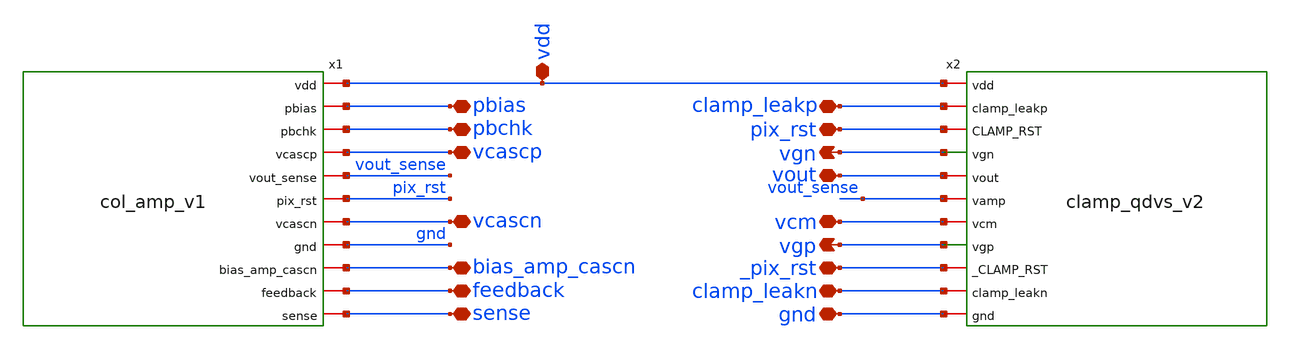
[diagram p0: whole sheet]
** sch_path: analog/xschem/col_amp_n_clamp_v1/analog_column_layout_schem.sch
**.subckt analog_column_layout_schem clamp_leakn gnd vdd vgn clamp_leakp vgp vcm vout pix_rst
*+ _pix_rst sense pbchk vcascp pbias feedback vcascn bias_amp_cascn
*.iopin clamp_leakn
*.iopin gnd
*.iopin vdd
*.opin vgn
*.iopin clamp_leakp
*.opin vgp
*.iopin vcm
*.iopin vout
*.iopin pix_rst
*.iopin _pix_rst
*.iopin sense
*.iopin pbchk
*.iopin vcascp
*.iopin pbias
*.iopin feedback
*.iopin vcascn
*.iopin bias_amp_cascn
x1 vdd pbias pbchk vcascp vout_sense pix_rst vcascn gnd bias_amp_cascn feedback sense col_amp_v1
x2 vdd clamp_leakp pix_rst vgn vout vout_sense vcm vgp _pix_rst clamp_leakn gnd clamp_qdvs_v2
**.ends

* expanding   symbol:
*+  /home/user/projects/nic2025_v2/nic2025_openDVS/analog/xschem/col_amp_n_clamp_v1/col_amp_v1.sym # of pins=11
** sym_path: analog/xschem/col_amp_n_clamp_v1/col_amp_v1.sym
** sch_path: analog/xschem/col_amp_n_clamp_v1/col_amp_v1.sch
.subckt col_amp_v1 vdd pbias pbchk vcascp vout_sense pix_rst vcascn gnd bias_amp_cascn feedback
+ sense
*.iopin vdd
*.iopin gnd
*.iopin sense
*.iopin vout_sense
*.iopin feedback
*.iopin pbchk
*.iopin pix_rst
*.iopin vcascn
*.iopin vcascp
*.iopin pbias
*.iopin bias_amp_cascn
XMpb pbchk pbias vdd vdd sky130_fd_pr__pfet_01v8 L=1 W=1.25 nf=1 ad='int((1 + 1)/2) * 1.25 / 1 * 0.29'
+ as='int((1 + 2)/2) * 1.25 / 1 * 0.29' pd='2*int((1 + 1)/2) * (1.25 / 1 + 0.29)' ps='2*int((1 + 2)/2) * (1.25 / 1 + 0.29)'
+ nrd='0.29 / 1.25 ' nrs='0.29 / 1.25 ' sa=0 sb=0 sd=0 mult=1 m=1
XMnc vout_sense amp_p_vg sense gnd sky130_fd_pr__nfet_01v8 L=1 W=0.75 nf=1 ad='int((1 + 1)/2) * 0.75 / 1 * 0.29'
+ as='int((1 + 2)/2) * 0.75 / 1 * 0.29' pd='2*int((1 + 1)/2) * (0.75 / 1 + 0.29)' ps='2*int((1 + 2)/2) * (0.75 / 1 + 0.29)'
+ nrd='0.29 / 0.75 ' nrs='0.29 / 0.75 ' sa=0 sb=0 sd=0 mult=1 m=1
XMfb vout_sense pix_rst feedback gnd sky130_fd_pr__nfet_01v8 L=0.5 W=0.5 nf=1 ad='int((1 + 1)/2) * 0.5 / 1 * 0.29'
+ as='int((1 + 2)/2) * 0.5 / 1 * 0.29' pd='2*int((1 + 1)/2) * (0.5 / 1 + 0.29)' ps='2*int((1 + 2)/2) * (0.5 / 1 + 0.29)'
+ nrd='0.29 / 0.5 ' nrs='0.29 / 0.5 ' sa=0 sb=0 sd=0 mult=1 m=1
XMpc vout_sense vcascp pbchk vdd sky130_fd_pr__pfet_01v8 L=1 W=1.25 nf=1 ad='int((1 + 1)/2) * 1.25 / 1 * 0.29'
+ as='int((1 + 2)/2) * 1.25 / 1 * 0.29' pd='2*int((1 + 1)/2) * (1.25 / 1 + 0.29)' ps='2*int((1 + 2)/2) * (1.25 / 1 + 0.29)'
+ nrd='0.29 / 1.25 ' nrs='0.29 / 1.25 ' sa=0 sb=0 sd=0 mult=1 m=1
XMpb1 pbchk pbias vdd vdd sky130_fd_pr__pfet_01v8 L=1 W=1.25 nf=1 ad='int((1 + 1)/2) * 1.25 / 1 * 0.29'
+ as='int((1 + 2)/2) * 1.25 / 1 * 0.29' pd='2*int((1 + 1)/2) * (1.25 / 1 + 0.29)' ps='2*int((1 + 2)/2) * (1.25 / 1 + 0.29)'
+ nrd='0.29 / 1.25 ' nrs='0.29 / 1.25 ' sa=0 sb=0 sd=0 mult=1 m=1
XMpc1 vout_sense vcascp pbchk vdd sky130_fd_pr__pfet_01v8 L=1 W=1.25 nf=1 ad='int((1 + 1)/2) * 1.25 / 1 * 0.29'
+ as='int((1 + 2)/2) * 1.25 / 1 * 0.29' pd='2*int((1 + 1)/2) * (1.25 / 1 + 0.29)' ps='2*int((1 + 2)/2) * (1.25 / 1 + 0.29)'
+ nrd='0.29 / 1.25 ' nrs='0.29 / 1.25 ' sa=0 sb=0 sd=0 mult=1 m=1
XMpb2 pbchk pbias vdd vdd sky130_fd_pr__pfet_01v8 L=1 W=1.25 nf=1 ad='int((1 + 1)/2) * 1.25 / 1 * 0.29'
+ as='int((1 + 2)/2) * 1.25 / 1 * 0.29' pd='2*int((1 + 1)/2) * (1.25 / 1 + 0.29)' ps='2*int((1 + 2)/2) * (1.25 / 1 + 0.29)'
+ nrd='0.29 / 1.25 ' nrs='0.29 / 1.25 ' sa=0 sb=0 sd=0 mult=1 m=1
XMpc2 vout_sense vcascp pbchk vdd sky130_fd_pr__pfet_01v8 L=1 W=1.25 nf=1 ad='int((1 + 1)/2) * 1.25 / 1 * 0.29'
+ as='int((1 + 2)/2) * 1.25 / 1 * 0.29' pd='2*int((1 + 1)/2) * (1.25 / 1 + 0.29)' ps='2*int((1 + 2)/2) * (1.25 / 1 + 0.29)'
+ nrd='0.29 / 1.25 ' nrs='0.29 / 1.25 ' sa=0 sb=0 sd=0 mult=1 m=1
XMpb3 pbchk pbias vdd vdd sky130_fd_pr__pfet_01v8 L=1 W=1.25 nf=1 ad='int((1 + 1)/2) * 1.25 / 1 * 0.29'
+ as='int((1 + 2)/2) * 1.25 / 1 * 0.29' pd='2*int((1 + 1)/2) * (1.25 / 1 + 0.29)' ps='2*int((1 + 2)/2) * (1.25 / 1 + 0.29)'
+ nrd='0.29 / 1.25 ' nrs='0.29 / 1.25 ' sa=0 sb=0 sd=0 mult=1 m=1
XMpc3 vout_sense vcascp pbchk vdd sky130_fd_pr__pfet_01v8 L=1 W=1.25 nf=1 ad='int((1 + 1)/2) * 1.25 / 1 * 0.29'
+ as='int((1 + 2)/2) * 1.25 / 1 * 0.29' pd='2*int((1 + 1)/2) * (1.25 / 1 + 0.29)' ps='2*int((1 + 2)/2) * (1.25 / 1 + 0.29)'
+ nrd='0.29 / 1.25 ' nrs='0.29 / 1.25 ' sa=0 sb=0 sd=0 mult=1 m=1
XMnc1 vout_sense amp_p_vg sense gnd sky130_fd_pr__nfet_01v8 L=1 W=0.75 nf=1 ad='int((1 + 1)/2) * 0.75 / 1 * 0.29'
+ as='int((1 + 2)/2) * 0.75 / 1 * 0.29' pd='2*int((1 + 1)/2) * (0.75 / 1 + 0.29)' ps='2*int((1 + 2)/2) * (0.75 / 1 + 0.29)'
+ nrd='0.29 / 0.75 ' nrs='0.29 / 0.75 ' sa=0 sb=0 sd=0 mult=1 m=1
XMnc2 vout_sense amp_p_vg sense gnd sky130_fd_pr__nfet_01v8 L=1 W=0.75 nf=1 ad='int((1 + 1)/2) * 0.75 / 1 * 0.29'
+ as='int((1 + 2)/2) * 0.75 / 1 * 0.29' pd='2*int((1 + 1)/2) * (0.75 / 1 + 0.29)' ps='2*int((1 + 2)/2) * (0.75 / 1 + 0.29)'
+ nrd='0.29 / 0.75 ' nrs='0.29 / 0.75 ' sa=0 sb=0 sd=0 mult=1 m=1
XMnc3 vout_sense amp_p_vg sense gnd sky130_fd_pr__nfet_01v8 L=1 W=0.75 nf=1 ad='int((1 + 1)/2) * 0.75 / 1 * 0.29'
+ as='int((1 + 2)/2) * 0.75 / 1 * 0.29' pd='2*int((1 + 1)/2) * (0.75 / 1 + 0.29)' ps='2*int((1 + 2)/2) * (0.75 / 1 + 0.29)'
+ nrd='0.29 / 0.75 ' nrs='0.29 / 0.75 ' sa=0 sb=0 sd=0 mult=1 m=1
xamp vdd amp_p_vg vcascn sense bias_amp_cascn gnd amp_p_5T
.ends


* expanding   symbol:
*+  /home/user/projects/nic2025_v2/nic2025_openDVS/analog/xschem/col_amp_n_clamp_v1/clamp_qdvs_v2.sym # of pins=11
** sym_path: analog/xschem/final/col_amp_n_clamp_v1/clamp_qdvs_v2.sym
** sch_path: analog/xschem/final/col_amp_n_clamp_v1/clamp_qdvs_v2.sch
.subckt clamp_qdvs_v2 vdd clamp_leakp CLAMP_RST vgn vout vamp vcm vgp _CLAMP_RST clamp_leakn gnd
*.iopin vdd
*.iopin gnd
*.iopin vcm
*.iopin _CLAMP_RST
*.iopin CLAMP_RST
*.iopin clamp_leakp
*.iopin clamp_leakn
*.iopin vout
*.iopin vamp
*.opin vgn
*.opin vgp
XM1 vgn vgn vcm gnd sky130_fd_pr__nfet_01v8 L=0.5 W=0.75 nf=1 ad='int((1 + 1)/2) * 0.75 / 1 * 0.29' as='int((1 + 2)/2) * 0.75 / 1 * 0.29'
+ pd='2*int((1 + 1)/2) * (0.75 / 1 + 0.29)' ps='2*int((1 + 2)/2) * (0.75 / 1 + 0.29)' nrd='0.29 / 0.75 '
+ nrs='0.29 / 0.75 ' sa=0 sb=0 sd=0 mult=1 m=1
XM2 vgp vgp vcm vdd sky130_fd_pr__pfet_01v8 L=0.5 W=1.5 nf=1 ad='int((1 + 1)/2) * 1.5 / 1 * 0.29' as='int((1 + 2)/2) * 1.5 / 1 * 0.29'
+ pd='2*int((1 + 1)/2) * (1.5 / 1 + 0.29)' ps='2*int((1 + 2)/2) * (1.5 / 1 + 0.29)' nrd='0.29 / 1.5 ' nrs='0.29 / 1.5 '
+ sa=0 sb=0 sd=0 mult=1 m=1
XM3 vgn clamp_leakp vdd vdd sky130_fd_pr__pfet_01v8 L=0.5 W=1.5 nf=1 ad='int((1 + 1)/2) * 1.5 / 1 * 0.29'
+ as='int((1 + 2)/2) * 1.5 / 1 * 0.29' pd='2*int((1 + 1)/2) * (1.5 / 1 + 0.29)' ps='2*int((1 + 2)/2) * (1.5 / 1 + 0.29)'
+ nrd='0.29 / 1.5 ' nrs='0.29 / 1.5 ' sa=0 sb=0 sd=0 mult=1 m=1
XM4 vgp clamp_leakn gnd gnd sky130_fd_pr__nfet_01v8 L=0.5 W=0.75 nf=1 ad='int((1 + 1)/2) * 0.75 / 1 * 0.29'
+ as='int((1 + 2)/2) * 0.75 / 1 * 0.29' pd='2*int((1 + 1)/2) * (0.75 / 1 + 0.29)' ps='2*int((1 + 2)/2) * (0.75 / 1 + 0.29)'
+ nrd='0.29 / 0.75 ' nrs='0.29 / 0.75 ' sa=0 sb=0 sd=0 mult=1 m=1
XM5 vdd vgn vout gnd sky130_fd_pr__nfet_01v8 L=0.5 W=0.75 nf=1 ad='int((1 + 1)/2) * 0.75 / 1 * 0.29'
+ as='int((1 + 2)/2) * 0.75 / 1 * 0.29' pd='2*int((1 + 1)/2) * (0.75 / 1 + 0.29)' ps='2*int((1 + 2)/2) * (0.75 / 1 + 0.29)'
+ nrd='0.29 / 0.75 ' nrs='0.29 / 0.75 ' sa=0 sb=0 sd=0 mult=1 m=1
XM6 gnd vgp vout vdd sky130_fd_pr__pfet_01v8 L=0.5 W=1.5 nf=1 ad='int((1 + 1)/2) * 1.5 / 1 * 0.29' as='int((1 + 2)/2) * 1.5 / 1 * 0.29'
+ pd='2*int((1 + 1)/2) * (1.5 / 1 + 0.29)' ps='2*int((1 + 2)/2) * (1.5 / 1 + 0.29)' nrd='0.29 / 1.5 ' nrs='0.29 / 1.5 '
+ sa=0 sb=0 sd=0 mult=1 m=1
XM7 vout _CLAMP_RST vamp gnd sky130_fd_pr__nfet_01v8 L=0.5 W=0.75 nf=1 ad='int((1 + 1)/2) * 0.75 / 1 * 0.29'
+ as='int((1 + 2)/2) * 0.75 / 1 * 0.29' pd='2*int((1 + 1)/2) * (0.75 / 1 + 0.29)' ps='2*int((1 + 2)/2) * (0.75 / 1 + 0.29)'
+ nrd='0.29 / 0.75 ' nrs='0.29 / 0.75 ' sa=0 sb=0 sd=0 mult=1 m=1
XM8 vout CLAMP_RST vamp vdd sky130_fd_pr__pfet_01v8 L=0.5 W=1.5 nf=1 ad='int((1 + 1)/2) * 1.5 / 1 * 0.29'
+ as='int((1 + 2)/2) * 1.5 / 1 * 0.29' pd='2*int((1 + 1)/2) * (1.5 / 1 + 0.29)' ps='2*int((1 + 2)/2) * (1.5 / 1 + 0.29)'
+ nrd='0.29 / 1.5 ' nrs='0.29 / 1.5 ' sa=0 sb=0 sd=0 mult=1 m=1
.ends


* expanding   symbol:  col_amp_n_clamp_v1/amp_p_5T.sym # of pins=6
** sym_path: analog/xschem/final/col_amp_n_clamp_v1/amp_p_5T.sym
** sch_path: analog/xschem/final/col_amp_n_clamp_v1/amp_p_5T.sch
.subckt amp_p_5T vdd vout vp vm vbias gnd
*.iopin gnd
*.iopin vdd
*.iopin vout
*.iopin vm
*.iopin vp
*.iopin vbias
XMinm vout vm vsource vdd sky130_fd_pr__pfet_01v8 L=0.2 W=0.5 nf=1 ad='int((1 + 1)/2) * 0.5 / 1 * 0.29'
+ as='int((1 + 2)/2) * 0.5 / 1 * 0.29' pd='2*int((1 + 1)/2) * (0.5 / 1 + 0.29)' ps='2*int((1 + 2)/2) * (0.5 / 1 + 0.29)'
+ nrd='0.29 / 0.5 ' nrs='0.29 / 0.5 ' sa=0 sb=0 sd=0 mult=1 m=1
XMinp vdio vp vsource vdd sky130_fd_pr__pfet_01v8 L=0.2 W=0.5 nf=1 ad='int((1 + 1)/2) * 0.5 / 1 * 0.29'
+ as='int((1 + 2)/2) * 0.5 / 1 * 0.29' pd='2*int((1 + 1)/2) * (0.5 / 1 + 0.29)' ps='2*int((1 + 2)/2) * (0.5 / 1 + 0.29)'
+ nrd='0.29 / 0.5 ' nrs='0.29 / 0.5 ' sa=0 sb=0 sd=0 mult=1 m=1
XMdio vdio vdio gnd gnd sky130_fd_pr__nfet_01v8 L=0.2 W=0.5 nf=1 ad='int((1 + 1)/2) * 0.5 / 1 * 0.29'
+ as='int((1 + 2)/2) * 0.5 / 1 * 0.29' pd='2*int((1 + 1)/2) * (0.5 / 1 + 0.29)' ps='2*int((1 + 2)/2) * (0.5 / 1 + 0.29)'
+ nrd='0.29 / 0.5 ' nrs='0.29 / 0.5 ' sa=0 sb=0 sd=0 mult=1 m=1
XMmirr vout vdio gnd gnd sky130_fd_pr__nfet_01v8 L=0.2 W=0.5 nf=1 ad='int((1 + 1)/2) * 0.5 / 1 * 0.29'
+ as='int((1 + 2)/2) * 0.5 / 1 * 0.29' pd='2*int((1 + 1)/2) * (0.5 / 1 + 0.29)' ps='2*int((1 + 2)/2) * (0.5 / 1 + 0.29)'
+ nrd='0.29 / 0.5 ' nrs='0.29 / 0.5 ' sa=0 sb=0 sd=0 mult=1 m=1
XMbias vsource vbias vdd vdd sky130_fd_pr__pfet_01v8 L=1 W=1 nf=1 ad='int((1 + 1)/2) * 1 / 1 * 0.29'
+ as='int((1 + 2)/2) * 1 / 1 * 0.29' pd='2*int((1 + 1)/2) * (1 / 1 + 0.29)' ps='2*int((1 + 2)/2) * (1 / 1 + 0.29)'
+ nrd='0.29 / 1 ' nrs='0.29 / 1 ' sa=0 sb=0 sd=0 mult=1 m=1
.ends

.end
